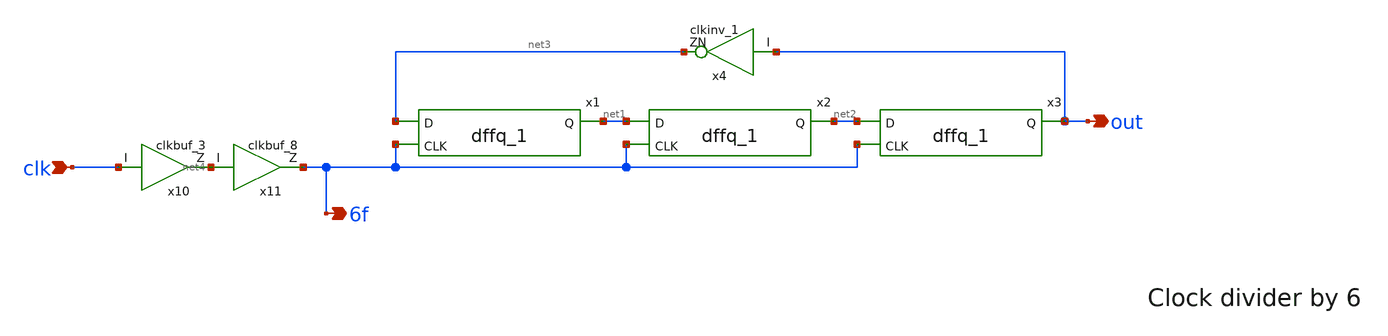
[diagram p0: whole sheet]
** sch_path: PLL/xschem/fdiv2.sch
**.subckt fdiv2 clk out 6f
*.ipin clk
*.opin out
*.opin 6f
x10 clk net4 VDD VDD 0 0 gf180mcu_fd_sc_mcu7t5v0__clkbuf_3
x11 net4 6f VDD VDD 0 0 gf180mcu_fd_sc_mcu7t5v0__clkbuf_8
x1 net3 6f net1 VDD VDD 0 0 gf180mcu_fd_sc_mcu7t5v0__dffq_1
x2 net1 6f net2 VDD VDD 0 0 gf180mcu_fd_sc_mcu7t5v0__dffq_1
x3 net2 6f out VDD VDD 0 0 gf180mcu_fd_sc_mcu7t5v0__dffq_1
x4 out net3 VDD VDD 0 0 gf180mcu_fd_sc_mcu7t5v0__clkinv_1
**.ends
.end
